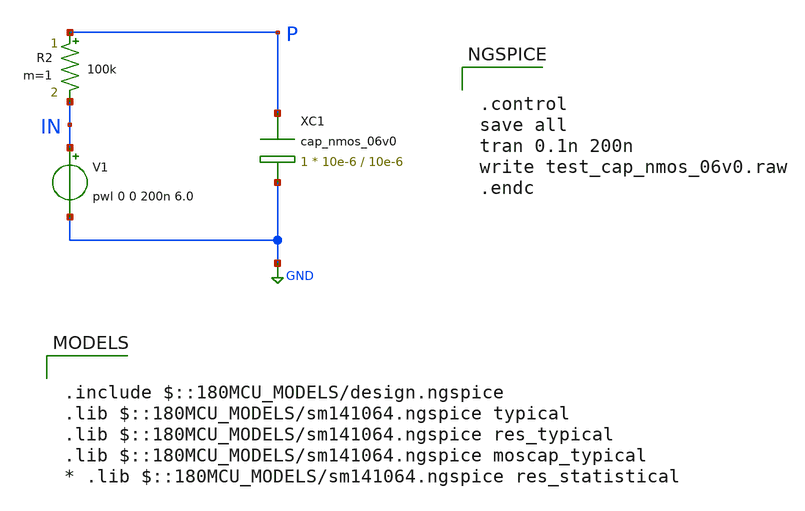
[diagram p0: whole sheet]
** sch_path: gf180mcuD/xschem_libs/gf180mcu_tests/test_cap_nmos_06v0/schematic/test_cap_nmos_06v0.sch
* Copyright 2022 GlobalFoundries PDK Authors
* Licensed under the Apache License, Version 2.0 (the "License");
* you may not use this file except in compliance with the License.
* You may obtain a copy of the License at
* https://www.apache.org/licenses/LICENSE-2.0
* Unless required by applicable law or agreed to in writing, software
* distributed under the License is distributed on an "AS IS" BASIS,
* WITHOUT WARRANTIES OR CONDITIONS OF ANY KIND, either express or implied.
* See the License for the specific language governing permissions and
* limitations under the License.
**.subckt test_cap_nmos_06v0
XC1 P GND cap_nmos_06v0 c_width=10e-6 c_length=10e-6 m=1
V1 IN GND pwl 0 0 200n 6.0
R2 P IN 100k m=1
**** begin user architecture code

.include $::180MCU_MODELS/design.ngspice
.lib $::180MCU_MODELS/sm141064.ngspice typical
.lib $::180MCU_MODELS/sm141064.ngspice res_typical
.lib $::180MCU_MODELS/sm141064.ngspice moscap_typical
* .lib $::180MCU_MODELS/sm141064.ngspice res_statistical



.control
save all
tran 0.1n 200n
write test_cap_nmos_06v0.raw
.endc


**** end user architecture code
**.ends
.GLOBAL GND
.end
